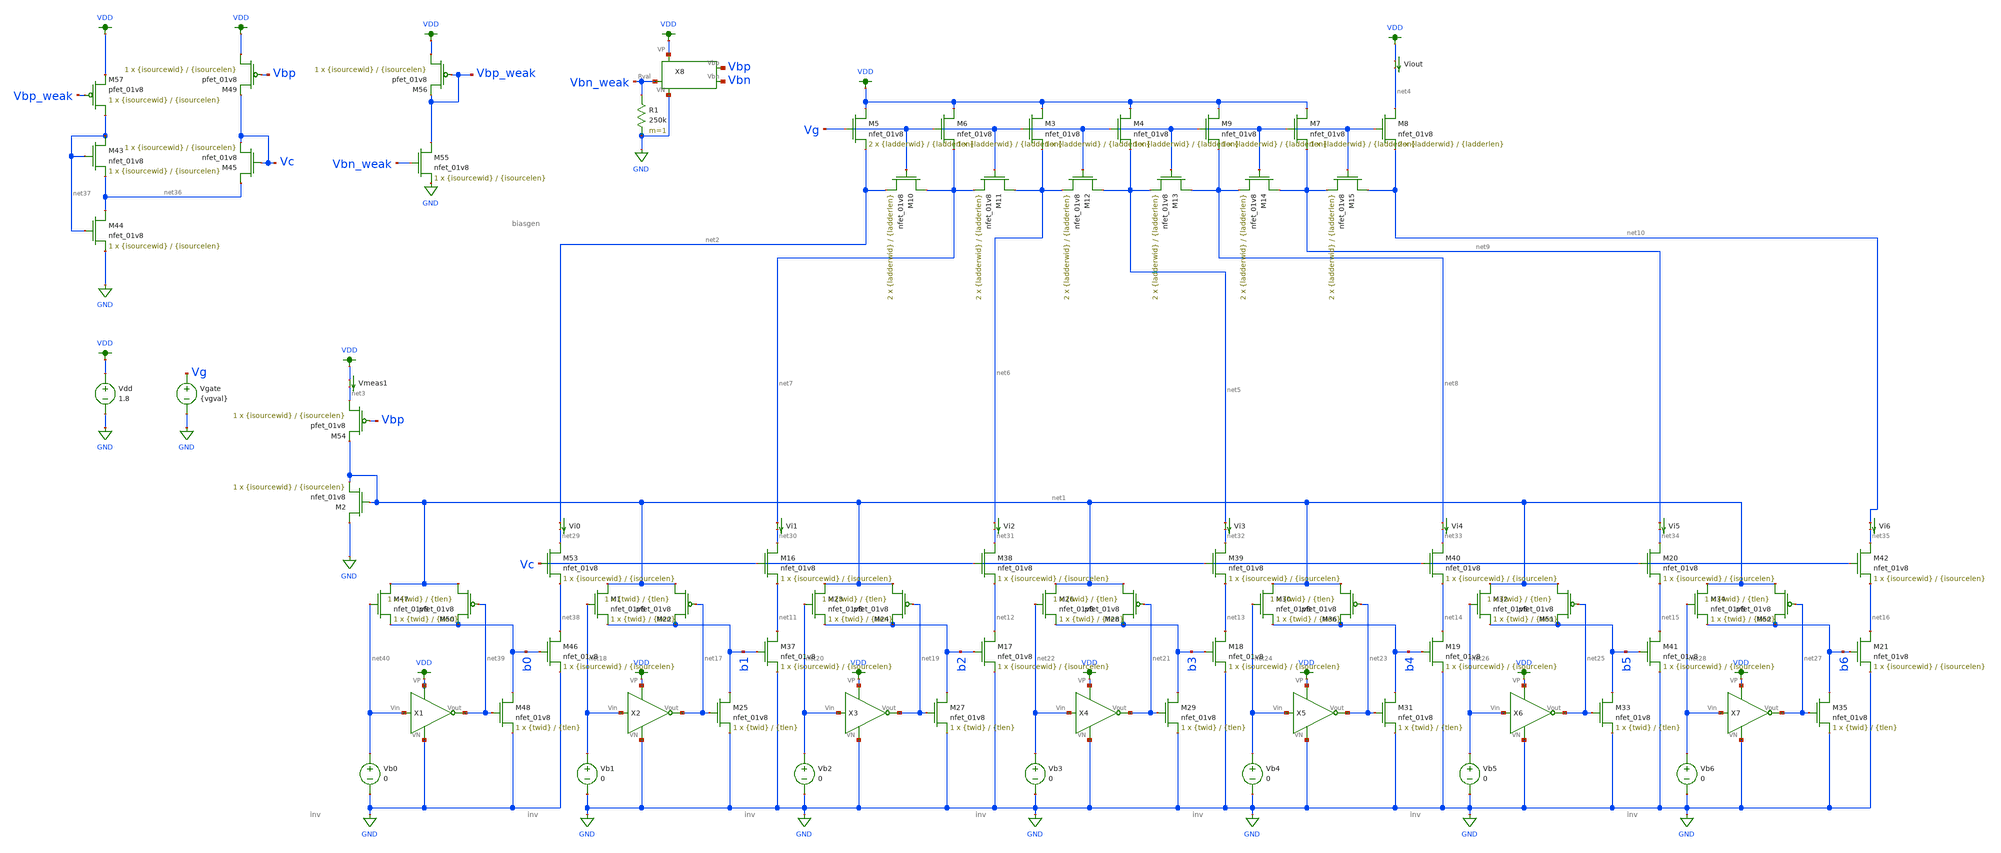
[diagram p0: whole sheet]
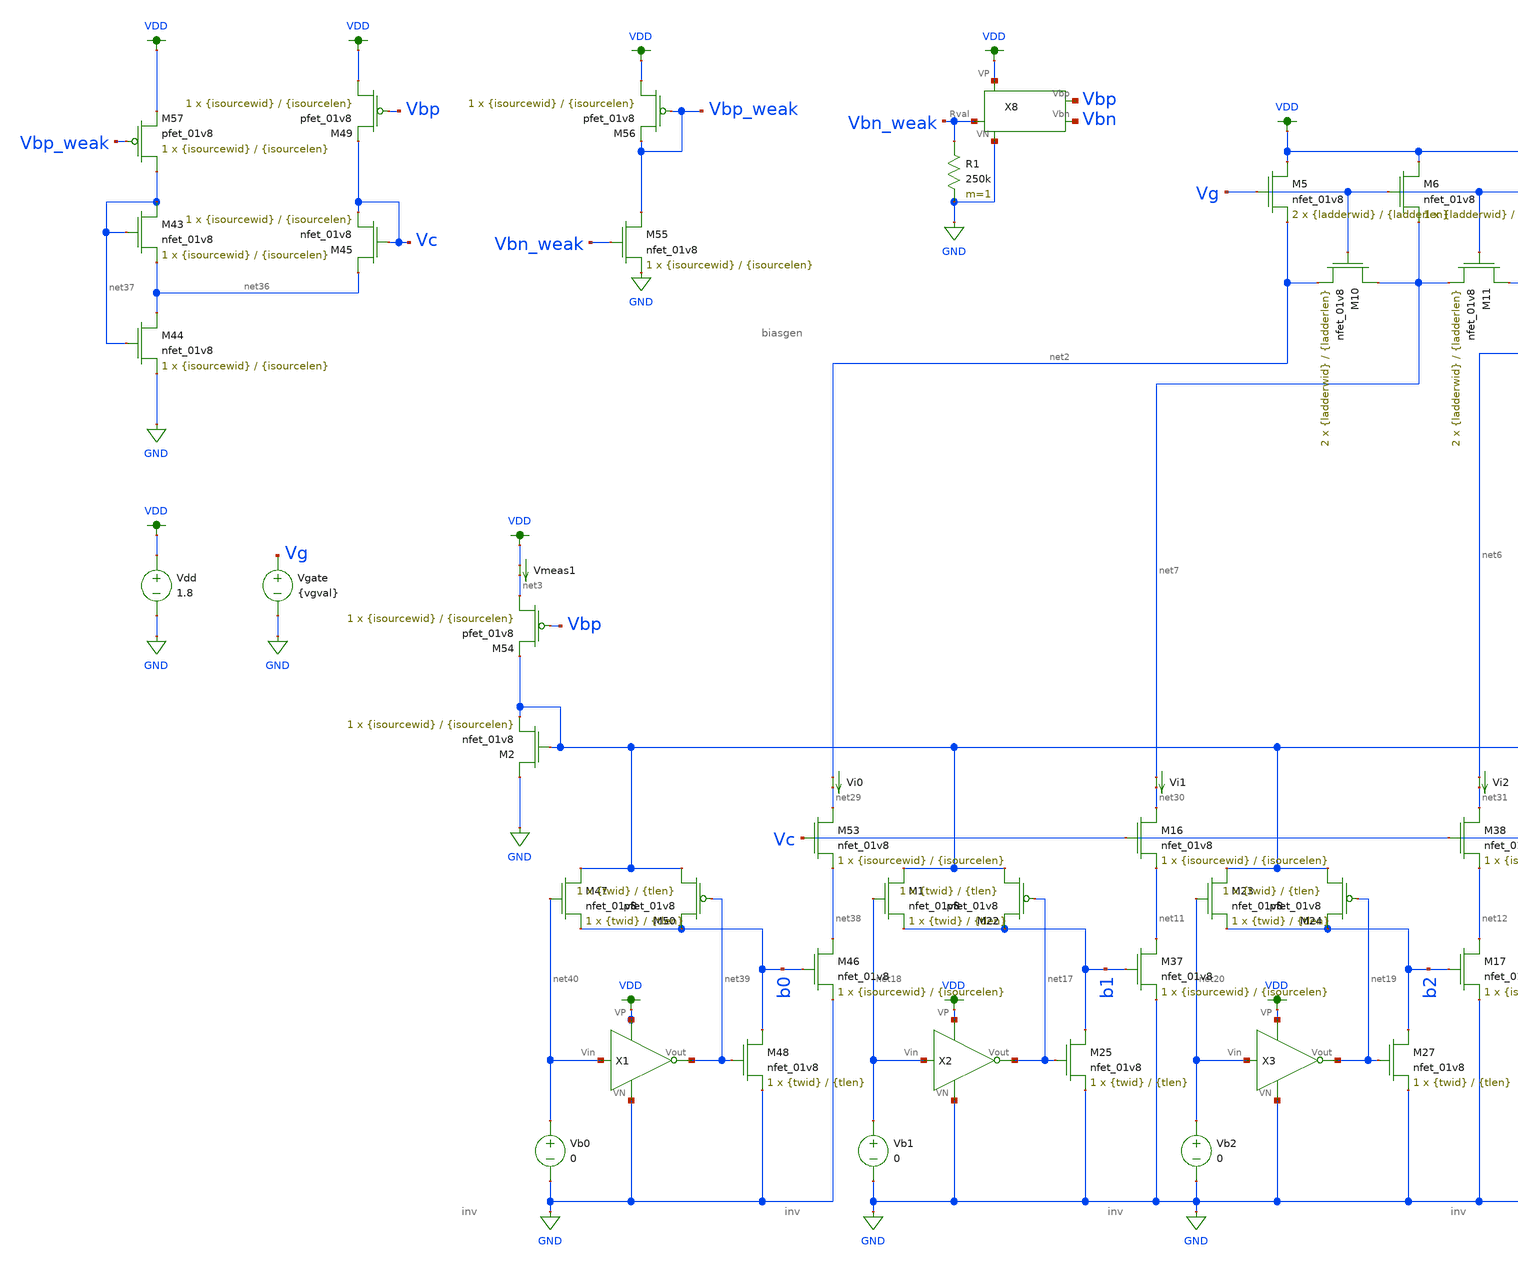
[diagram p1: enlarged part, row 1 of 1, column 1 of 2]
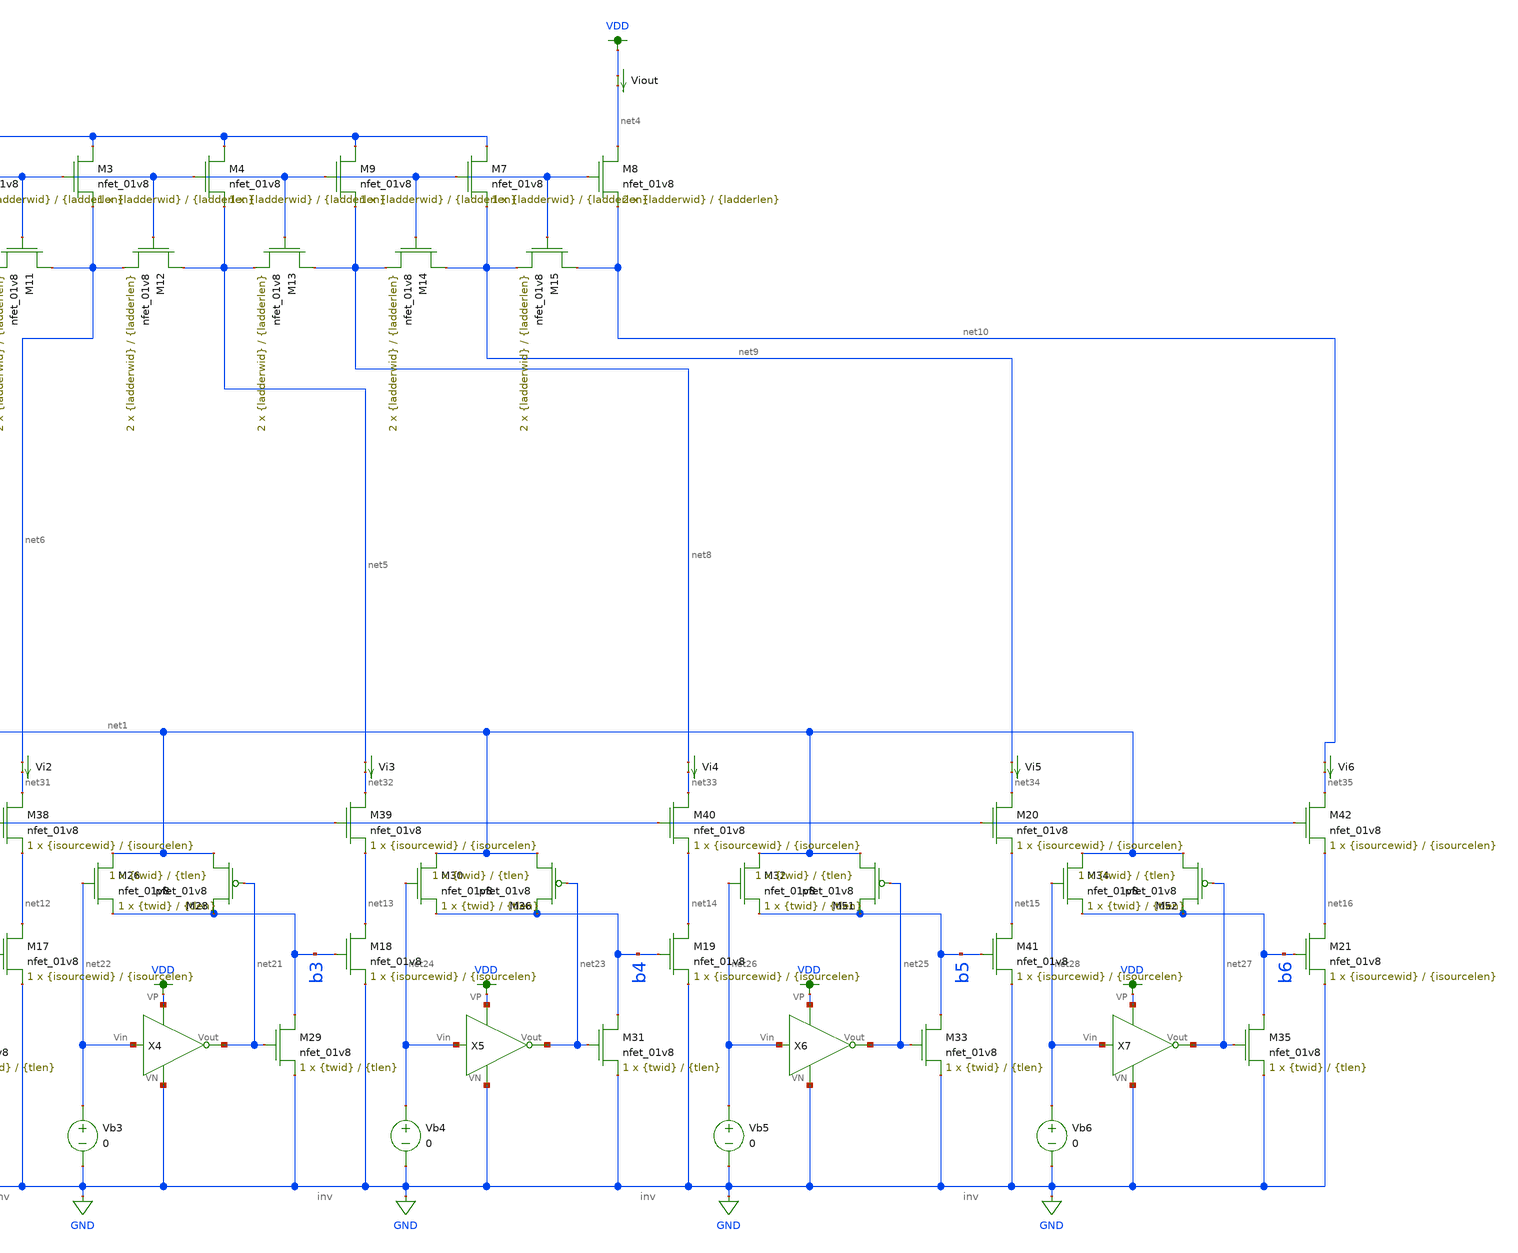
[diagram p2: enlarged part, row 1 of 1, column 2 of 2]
** sch_path: prelim-files/testing.sch
**.subckt testing
XM2 GND net1 net1 GND sky130_fd_pr__nfet_01v8 L={isourcelen} W={isourcewid} nf=1 ad='int((nf+1)/2) * W/nf * 0.29'
+ as='int((nf+2)/2) * W/nf * 0.29' pd='2*int((nf+1)/2) * (W/nf + 0.29)' ps='2*int((nf+2)/2) * (W/nf + 0.29)'
+ nrd='0.29 / W' nrs='0.29 / W' sa=0 sb=0 sd=0 mult=1 m=1
Vdd VDD GND 1.8
Vi0 net2 net29 0
.save i(vi0)
Vmeas1 VDD net3 0
.save i(vmeas1)
XM5 VDD Vg net2 GND sky130_fd_pr__nfet_01v8 L={ladderlen} W={ladderwid} nf=1 ad='int((nf+1)/2) * W/nf * 0.29'
+ as='int((nf+2)/2) * W/nf * 0.29' pd='2*int((nf+1)/2) * (W/nf + 0.29)' ps='2*int((nf+2)/2) * (W/nf + 0.29)'
+ nrd='0.29 / W' nrs='0.29 / W' sa=0 sb=0 sd=0 mult=2 m=2
XM6 VDD Vg net7 GND sky130_fd_pr__nfet_01v8 L={ladderlen} W={ladderwid} nf=1 ad='int((nf+1)/2) * W/nf * 0.29'
+ as='int((nf+2)/2) * W/nf * 0.29' pd='2*int((nf+1)/2) * (W/nf + 0.29)' ps='2*int((nf+2)/2) * (W/nf + 0.29)'
+ nrd='0.29 / W' nrs='0.29 / W' sa=0 sb=0 sd=0 mult=1 m=1
Viout VDD net4 0
.save i(viout)
Vb1 net18 GND 0
Vb2 net20 GND 0
Vgate Vg GND {vgval}
Vi1 net7 net30 0
.save i(vi1)
Vi2 net6 net31 0
.save i(vi2)
Vb3 net22 GND 0
Vi3 net5 net32 0
.save i(vi3)
Vb4 net24 GND 0
Vi4 net8 net33 0
.save i(vi4)
Vb5 net26 GND 0
Vi5 net9 net34 0
.save i(vi5)
Vb6 net28 GND 0
Vi6 net10 net35 0
.save i(vi6)
X2 net18 net17 VDD GND inv
XM25 b1 net17 GND GND sky130_fd_pr__nfet_01v8 L={tlen} W={twid} nf=1 ad='int((nf+1)/2) * W/nf * 0.29'
+ as='int((nf+2)/2) * W/nf * 0.29' pd='2*int((nf+1)/2) * (W/nf + 0.29)' ps='2*int((nf+2)/2) * (W/nf + 0.29)'
+ nrd='0.29 / W' nrs='0.29 / W' sa=0 sb=0 sd=0 mult=1 m=1
X3 net20 net19 VDD GND inv
XM27 b2 net19 GND GND sky130_fd_pr__nfet_01v8 L={tlen} W={twid} nf=1 ad='int((nf+1)/2) * W/nf * 0.29'
+ as='int((nf+2)/2) * W/nf * 0.29' pd='2*int((nf+1)/2) * (W/nf + 0.29)' ps='2*int((nf+2)/2) * (W/nf + 0.29)'
+ nrd='0.29 / W' nrs='0.29 / W' sa=0 sb=0 sd=0 mult=1 m=1
X4 net22 net21 VDD GND inv
XM29 b3 net21 GND GND sky130_fd_pr__nfet_01v8 L={tlen} W={twid} nf=1 ad='int((nf+1)/2) * W/nf * 0.29'
+ as='int((nf+2)/2) * W/nf * 0.29' pd='2*int((nf+1)/2) * (W/nf + 0.29)' ps='2*int((nf+2)/2) * (W/nf + 0.29)'
+ nrd='0.29 / W' nrs='0.29 / W' sa=0 sb=0 sd=0 mult=1 m=1
X5 net24 net23 VDD GND inv
XM31 b4 net23 GND GND sky130_fd_pr__nfet_01v8 L={tlen} W={twid} nf=1 ad='int((nf+1)/2) * W/nf * 0.29'
+ as='int((nf+2)/2) * W/nf * 0.29' pd='2*int((nf+1)/2) * (W/nf + 0.29)' ps='2*int((nf+2)/2) * (W/nf + 0.29)'
+ nrd='0.29 / W' nrs='0.29 / W' sa=0 sb=0 sd=0 mult=1 m=1
X6 net26 net25 VDD GND inv
XM33 b5 net25 GND GND sky130_fd_pr__nfet_01v8 L={tlen} W={twid} nf=1 ad='int((nf+1)/2) * W/nf * 0.29'
+ as='int((nf+2)/2) * W/nf * 0.29' pd='2*int((nf+1)/2) * (W/nf + 0.29)' ps='2*int((nf+2)/2) * (W/nf + 0.29)'
+ nrd='0.29 / W' nrs='0.29 / W' sa=0 sb=0 sd=0 mult=1 m=1
X7 net28 net27 VDD GND inv
XM35 b6 net27 GND GND sky130_fd_pr__nfet_01v8 L={tlen} W={twid} nf=1 ad='int((nf+1)/2) * W/nf * 0.29'
+ as='int((nf+2)/2) * W/nf * 0.29' pd='2*int((nf+1)/2) * (W/nf + 0.29)' ps='2*int((nf+2)/2) * (W/nf + 0.29)'
+ nrd='0.29 / W' nrs='0.29 / W' sa=0 sb=0 sd=0 mult=1 m=1
XM43 net37 net37 net36 GND sky130_fd_pr__nfet_01v8 L={isourcelen} W={isourcewid} nf=1 ad='int((nf+1)/2) * W/nf * 0.29'
+ as='int((nf+2)/2) * W/nf * 0.29' pd='2*int((nf+1)/2) * (W/nf + 0.29)' ps='2*int((nf+2)/2) * (W/nf + 0.29)'
+ nrd='0.29 / W' nrs='0.29 / W' sa=0 sb=0 sd=0 mult=1 m=1
XM44 net36 net37 GND GND sky130_fd_pr__nfet_01v8 L={isourcelen} W={isourcewid} nf=1 ad='int((nf+1)/2) * W/nf * 0.29'
+ as='int((nf+2)/2) * W/nf * 0.29' pd='2*int((nf+1)/2) * (W/nf + 0.29)' ps='2*int((nf+2)/2) * (W/nf + 0.29)'
+ nrd='0.29 / W' nrs='0.29 / W' sa=0 sb=0 sd=0 mult=1 m=1
XM45 net36 Vc Vc GND sky130_fd_pr__nfet_01v8 L={isourcelen} W={isourcewid} nf=1 ad='int((nf+1)/2) * W/nf * 0.29'
+ as='int((nf+2)/2) * W/nf * 0.29' pd='2*int((nf+1)/2) * (W/nf + 0.29)' ps='2*int((nf+2)/2) * (W/nf + 0.29)'
+ nrd='0.29 / W' nrs='0.29 / W' sa=0 sb=0 sd=0 mult=1 m=1
Vb0 net40 GND 0
X1 net40 net39 VDD GND inv
XM47 net1 net40 b0 GND sky130_fd_pr__nfet_01v8 L={tlen} W={twid} nf=1 ad='int((nf+1)/2) * W/nf * 0.29'
+ as='int((nf+2)/2) * W/nf * 0.29' pd='2*int((nf+1)/2) * (W/nf + 0.29)' ps='2*int((nf+2)/2) * (W/nf + 0.29)'
+ nrd='0.29 / W' nrs='0.29 / W' sa=0 sb=0 sd=0 mult=1 m=1
XM48 b0 net39 GND GND sky130_fd_pr__nfet_01v8 L={tlen} W={twid} nf=1 ad='int((nf+1)/2) * W/nf * 0.29'
+ as='int((nf+2)/2) * W/nf * 0.29' pd='2*int((nf+1)/2) * (W/nf + 0.29)' ps='2*int((nf+2)/2) * (W/nf + 0.29)'
+ nrd='0.29 / W' nrs='0.29 / W' sa=0 sb=0 sd=0 mult=1 m=1
XM50 net1 net39 b0 VDD sky130_fd_pr__pfet_01v8 L={tlen} W={twid} nf=1 ad='int((nf+1)/2) * W/nf * 0.29'
+ as='int((nf+2)/2) * W/nf * 0.29' pd='2*int((nf+1)/2) * (W/nf + 0.29)' ps='2*int((nf+2)/2) * (W/nf + 0.29)'
+ nrd='0.29 / W' nrs='0.29 / W' sa=0 sb=0 sd=0 mult=1 m=1
XM1 net1 net18 b1 GND sky130_fd_pr__nfet_01v8 L={tlen} W={twid} nf=1 ad='int((nf+1)/2) * W/nf * 0.29'
+ as='int((nf+2)/2) * W/nf * 0.29' pd='2*int((nf+1)/2) * (W/nf + 0.29)' ps='2*int((nf+2)/2) * (W/nf + 0.29)'
+ nrd='0.29 / W' nrs='0.29 / W' sa=0 sb=0 sd=0 mult=1 m=1
XM22 net1 net17 b1 VDD sky130_fd_pr__pfet_01v8 L={tlen} W={twid} nf=1 ad='int((nf+1)/2) * W/nf * 0.29'
+ as='int((nf+2)/2) * W/nf * 0.29' pd='2*int((nf+1)/2) * (W/nf + 0.29)' ps='2*int((nf+2)/2) * (W/nf + 0.29)'
+ nrd='0.29 / W' nrs='0.29 / W' sa=0 sb=0 sd=0 mult=1 m=1
XM23 net1 net20 b2 GND sky130_fd_pr__nfet_01v8 L={tlen} W={twid} nf=1 ad='int((nf+1)/2) * W/nf * 0.29'
+ as='int((nf+2)/2) * W/nf * 0.29' pd='2*int((nf+1)/2) * (W/nf + 0.29)' ps='2*int((nf+2)/2) * (W/nf + 0.29)'
+ nrd='0.29 / W' nrs='0.29 / W' sa=0 sb=0 sd=0 mult=1 m=1
XM24 net1 net19 b2 VDD sky130_fd_pr__pfet_01v8 L={tlen} W={twid} nf=1 ad='int((nf+1)/2) * W/nf * 0.29'
+ as='int((nf+2)/2) * W/nf * 0.29' pd='2*int((nf+1)/2) * (W/nf + 0.29)' ps='2*int((nf+2)/2) * (W/nf + 0.29)'
+ nrd='0.29 / W' nrs='0.29 / W' sa=0 sb=0 sd=0 mult=1 m=1
XM26 net1 net22 b3 GND sky130_fd_pr__nfet_01v8 L={tlen} W={twid} nf=1 ad='int((nf+1)/2) * W/nf * 0.29'
+ as='int((nf+2)/2) * W/nf * 0.29' pd='2*int((nf+1)/2) * (W/nf + 0.29)' ps='2*int((nf+2)/2) * (W/nf + 0.29)'
+ nrd='0.29 / W' nrs='0.29 / W' sa=0 sb=0 sd=0 mult=1 m=1
XM28 net1 net21 b3 VDD sky130_fd_pr__pfet_01v8 L={tlen} W={twid} nf=1 ad='int((nf+1)/2) * W/nf * 0.29'
+ as='int((nf+2)/2) * W/nf * 0.29' pd='2*int((nf+1)/2) * (W/nf + 0.29)' ps='2*int((nf+2)/2) * (W/nf + 0.29)'
+ nrd='0.29 / W' nrs='0.29 / W' sa=0 sb=0 sd=0 mult=1 m=1
XM30 net1 net24 b4 GND sky130_fd_pr__nfet_01v8 L={tlen} W={twid} nf=1 ad='int((nf+1)/2) * W/nf * 0.29'
+ as='int((nf+2)/2) * W/nf * 0.29' pd='2*int((nf+1)/2) * (W/nf + 0.29)' ps='2*int((nf+2)/2) * (W/nf + 0.29)'
+ nrd='0.29 / W' nrs='0.29 / W' sa=0 sb=0 sd=0 mult=1 m=1
XM36 net1 net23 b4 VDD sky130_fd_pr__pfet_01v8 L={tlen} W={twid} nf=1 ad='int((nf+1)/2) * W/nf * 0.29'
+ as='int((nf+2)/2) * W/nf * 0.29' pd='2*int((nf+1)/2) * (W/nf + 0.29)' ps='2*int((nf+2)/2) * (W/nf + 0.29)'
+ nrd='0.29 / W' nrs='0.29 / W' sa=0 sb=0 sd=0 mult=1 m=1
XM32 net1 net26 b5 GND sky130_fd_pr__nfet_01v8 L={tlen} W={twid} nf=1 ad='int((nf+1)/2) * W/nf * 0.29'
+ as='int((nf+2)/2) * W/nf * 0.29' pd='2*int((nf+1)/2) * (W/nf + 0.29)' ps='2*int((nf+2)/2) * (W/nf + 0.29)'
+ nrd='0.29 / W' nrs='0.29 / W' sa=0 sb=0 sd=0 mult=1 m=1
XM51 net1 net25 b5 VDD sky130_fd_pr__pfet_01v8 L={tlen} W={twid} nf=1 ad='int((nf+1)/2) * W/nf * 0.29'
+ as='int((nf+2)/2) * W/nf * 0.29' pd='2*int((nf+1)/2) * (W/nf + 0.29)' ps='2*int((nf+2)/2) * (W/nf + 0.29)'
+ nrd='0.29 / W' nrs='0.29 / W' sa=0 sb=0 sd=0 mult=1 m=1
XM34 net1 net28 b6 GND sky130_fd_pr__nfet_01v8 L={tlen} W={twid} nf=1 ad='int((nf+1)/2) * W/nf * 0.29'
+ as='int((nf+2)/2) * W/nf * 0.29' pd='2*int((nf+1)/2) * (W/nf + 0.29)' ps='2*int((nf+2)/2) * (W/nf + 0.29)'
+ nrd='0.29 / W' nrs='0.29 / W' sa=0 sb=0 sd=0 mult=1 m=1
XM52 net1 net27 b6 VDD sky130_fd_pr__pfet_01v8 L={tlen} W={twid} nf=1 ad='int((nf+1)/2) * W/nf * 0.29'
+ as='int((nf+2)/2) * W/nf * 0.29' pd='2*int((nf+1)/2) * (W/nf + 0.29)' ps='2*int((nf+2)/2) * (W/nf + 0.29)'
+ nrd='0.29 / W' nrs='0.29 / W' sa=0 sb=0 sd=0 mult=1 m=1
XM10 net7 Vg net2 GND sky130_fd_pr__nfet_01v8 L={ladderlen} W={ladderwid} nf=1 ad='int((nf+1)/2) * W/nf * 0.29'
+ as='int((nf+2)/2) * W/nf * 0.29' pd='2*int((nf+1)/2) * (W/nf + 0.29)' ps='2*int((nf+2)/2) * (W/nf + 0.29)'
+ nrd='0.29 / W' nrs='0.29 / W' sa=0 sb=0 sd=0 mult=2 m=2
XM11 net6 Vg net7 GND sky130_fd_pr__nfet_01v8 L={ladderlen} W={ladderwid} nf=1 ad='int((nf+1)/2) * W/nf * 0.29'
+ as='int((nf+2)/2) * W/nf * 0.29' pd='2*int((nf+1)/2) * (W/nf + 0.29)' ps='2*int((nf+2)/2) * (W/nf + 0.29)'
+ nrd='0.29 / W' nrs='0.29 / W' sa=0 sb=0 sd=0 mult=2 m=2
XM12 net5 Vg net6 GND sky130_fd_pr__nfet_01v8 L={ladderlen} W={ladderwid} nf=1 ad='int((nf+1)/2) * W/nf * 0.29'
+ as='int((nf+2)/2) * W/nf * 0.29' pd='2*int((nf+1)/2) * (W/nf + 0.29)' ps='2*int((nf+2)/2) * (W/nf + 0.29)'
+ nrd='0.29 / W' nrs='0.29 / W' sa=0 sb=0 sd=0 mult=2 m=2
XM13 net8 Vg net5 GND sky130_fd_pr__nfet_01v8 L={ladderlen} W={ladderwid} nf=1 ad='int((nf+1)/2) * W/nf * 0.29'
+ as='int((nf+2)/2) * W/nf * 0.29' pd='2*int((nf+1)/2) * (W/nf + 0.29)' ps='2*int((nf+2)/2) * (W/nf + 0.29)'
+ nrd='0.29 / W' nrs='0.29 / W' sa=0 sb=0 sd=0 mult=2 m=2
XM14 net9 Vg net8 GND sky130_fd_pr__nfet_01v8 L={ladderlen} W={ladderwid} nf=1 ad='int((nf+1)/2) * W/nf * 0.29'
+ as='int((nf+2)/2) * W/nf * 0.29' pd='2*int((nf+1)/2) * (W/nf + 0.29)' ps='2*int((nf+2)/2) * (W/nf + 0.29)'
+ nrd='0.29 / W' nrs='0.29 / W' sa=0 sb=0 sd=0 mult=2 m=2
XM15 net10 Vg net9 GND sky130_fd_pr__nfet_01v8 L={ladderlen} W={ladderwid} nf=1 ad='int((nf+1)/2) * W/nf * 0.29'
+ as='int((nf+2)/2) * W/nf * 0.29' pd='2*int((nf+1)/2) * (W/nf + 0.29)' ps='2*int((nf+2)/2) * (W/nf + 0.29)'
+ nrd='0.29 / W' nrs='0.29 / W' sa=0 sb=0 sd=0 mult=2 m=2
XM8 net4 Vg net10 GND sky130_fd_pr__nfet_01v8 L={ladderlen} W={ladderwid} nf=1 ad='int((nf+1)/2) * W/nf * 0.29'
+ as='int((nf+2)/2) * W/nf * 0.29' pd='2*int((nf+1)/2) * (W/nf + 0.29)' ps='2*int((nf+2)/2) * (W/nf + 0.29)'
+ nrd='0.29 / W' nrs='0.29 / W' sa=0 sb=0 sd=0 mult=2 m=2
XM3 VDD Vg net6 GND sky130_fd_pr__nfet_01v8 L={ladderlen} W={ladderwid} nf=1 ad='int((nf+1)/2) * W/nf * 0.29'
+ as='int((nf+2)/2) * W/nf * 0.29' pd='2*int((nf+1)/2) * (W/nf + 0.29)' ps='2*int((nf+2)/2) * (W/nf + 0.29)'
+ nrd='0.29 / W' nrs='0.29 / W' sa=0 sb=0 sd=0 mult=1 m=1
XM4 VDD Vg net5 GND sky130_fd_pr__nfet_01v8 L={ladderlen} W={ladderwid} nf=1 ad='int((nf+1)/2) * W/nf * 0.29'
+ as='int((nf+2)/2) * W/nf * 0.29' pd='2*int((nf+1)/2) * (W/nf + 0.29)' ps='2*int((nf+2)/2) * (W/nf + 0.29)'
+ nrd='0.29 / W' nrs='0.29 / W' sa=0 sb=0 sd=0 mult=1 m=1
XM9 VDD Vg net8 GND sky130_fd_pr__nfet_01v8 L={ladderlen} W={ladderwid} nf=1 ad='int((nf+1)/2) * W/nf * 0.29'
+ as='int((nf+2)/2) * W/nf * 0.29' pd='2*int((nf+1)/2) * (W/nf + 0.29)' ps='2*int((nf+2)/2) * (W/nf + 0.29)'
+ nrd='0.29 / W' nrs='0.29 / W' sa=0 sb=0 sd=0 mult=1 m=1
XM7 VDD Vg net9 GND sky130_fd_pr__nfet_01v8 L={ladderlen} W={ladderwid} nf=1 ad='int((nf+1)/2) * W/nf * 0.29'
+ as='int((nf+2)/2) * W/nf * 0.29' pd='2*int((nf+1)/2) * (W/nf + 0.29)' ps='2*int((nf+2)/2) * (W/nf + 0.29)'
+ nrd='0.29 / W' nrs='0.29 / W' sa=0 sb=0 sd=0 mult=1 m=1
XM53 net29 Vc net38 GND sky130_fd_pr__nfet_01v8 L={isourcelen} W={isourcewid} nf=1 ad='int((nf+1)/2) * W/nf * 0.29'
+ as='int((nf+2)/2) * W/nf * 0.29' pd='2*int((nf+1)/2) * (W/nf + 0.29)' ps='2*int((nf+2)/2) * (W/nf + 0.29)'
+ nrd='0.29 / W' nrs='0.29 / W' sa=0 sb=0 sd=0 mult=1 m=1
XM46 net38 b0 GND GND sky130_fd_pr__nfet_01v8 L={isourcelen} W={isourcewid} nf=1 ad='int((nf+1)/2) * W/nf * 0.29'
+ as='int((nf+2)/2) * W/nf * 0.29' pd='2*int((nf+1)/2) * (W/nf + 0.29)' ps='2*int((nf+2)/2) * (W/nf + 0.29)'
+ nrd='0.29 / W' nrs='0.29 / W' sa=0 sb=0 sd=0 mult=1 m=1
XM37 net11 b1 GND GND sky130_fd_pr__nfet_01v8 L={isourcelen} W={isourcewid} nf=1 ad='int((nf+1)/2) * W/nf * 0.29'
+ as='int((nf+2)/2) * W/nf * 0.29' pd='2*int((nf+1)/2) * (W/nf + 0.29)' ps='2*int((nf+2)/2) * (W/nf + 0.29)'
+ nrd='0.29 / W' nrs='0.29 / W' sa=0 sb=0 sd=0 mult=1 m=1
XM16 net30 Vc net11 GND sky130_fd_pr__nfet_01v8 L={isourcelen} W={isourcewid} nf=1 ad='int((nf+1)/2) * W/nf * 0.29'
+ as='int((nf+2)/2) * W/nf * 0.29' pd='2*int((nf+1)/2) * (W/nf + 0.29)' ps='2*int((nf+2)/2) * (W/nf + 0.29)'
+ nrd='0.29 / W' nrs='0.29 / W' sa=0 sb=0 sd=0 mult=1 m=1
XM17 net12 b2 GND GND sky130_fd_pr__nfet_01v8 L={isourcelen} W={isourcewid} nf=1 ad='int((nf+1)/2) * W/nf * 0.29'
+ as='int((nf+2)/2) * W/nf * 0.29' pd='2*int((nf+1)/2) * (W/nf + 0.29)' ps='2*int((nf+2)/2) * (W/nf + 0.29)'
+ nrd='0.29 / W' nrs='0.29 / W' sa=0 sb=0 sd=0 mult=1 m=1
XM38 net31 Vc net12 GND sky130_fd_pr__nfet_01v8 L={isourcelen} W={isourcewid} nf=1 ad='int((nf+1)/2) * W/nf * 0.29'
+ as='int((nf+2)/2) * W/nf * 0.29' pd='2*int((nf+1)/2) * (W/nf + 0.29)' ps='2*int((nf+2)/2) * (W/nf + 0.29)'
+ nrd='0.29 / W' nrs='0.29 / W' sa=0 sb=0 sd=0 mult=1 m=1
XM18 net13 b3 GND GND sky130_fd_pr__nfet_01v8 L={isourcelen} W={isourcewid} nf=1 ad='int((nf+1)/2) * W/nf * 0.29'
+ as='int((nf+2)/2) * W/nf * 0.29' pd='2*int((nf+1)/2) * (W/nf + 0.29)' ps='2*int((nf+2)/2) * (W/nf + 0.29)'
+ nrd='0.29 / W' nrs='0.29 / W' sa=0 sb=0 sd=0 mult=1 m=1
XM39 net32 Vc net13 GND sky130_fd_pr__nfet_01v8 L={isourcelen} W={isourcewid} nf=1 ad='int((nf+1)/2) * W/nf * 0.29'
+ as='int((nf+2)/2) * W/nf * 0.29' pd='2*int((nf+1)/2) * (W/nf + 0.29)' ps='2*int((nf+2)/2) * (W/nf + 0.29)'
+ nrd='0.29 / W' nrs='0.29 / W' sa=0 sb=0 sd=0 mult=1 m=1
XM19 net14 b4 GND GND sky130_fd_pr__nfet_01v8 L={isourcelen} W={isourcewid} nf=1 ad='int((nf+1)/2) * W/nf * 0.29'
+ as='int((nf+2)/2) * W/nf * 0.29' pd='2*int((nf+1)/2) * (W/nf + 0.29)' ps='2*int((nf+2)/2) * (W/nf + 0.29)'
+ nrd='0.29 / W' nrs='0.29 / W' sa=0 sb=0 sd=0 mult=1 m=1
XM40 net33 Vc net14 GND sky130_fd_pr__nfet_01v8 L={isourcelen} W={isourcewid} nf=1 ad='int((nf+1)/2) * W/nf * 0.29'
+ as='int((nf+2)/2) * W/nf * 0.29' pd='2*int((nf+1)/2) * (W/nf + 0.29)' ps='2*int((nf+2)/2) * (W/nf + 0.29)'
+ nrd='0.29 / W' nrs='0.29 / W' sa=0 sb=0 sd=0 mult=1 m=1
XM20 net34 Vc net15 GND sky130_fd_pr__nfet_01v8 L={isourcelen} W={isourcewid} nf=1 ad='int((nf+1)/2) * W/nf * 0.29'
+ as='int((nf+2)/2) * W/nf * 0.29' pd='2*int((nf+1)/2) * (W/nf + 0.29)' ps='2*int((nf+2)/2) * (W/nf + 0.29)'
+ nrd='0.29 / W' nrs='0.29 / W' sa=0 sb=0 sd=0 mult=1 m=1
XM41 net15 b5 GND GND sky130_fd_pr__nfet_01v8 L={isourcelen} W={isourcewid} nf=1 ad='int((nf+1)/2) * W/nf * 0.29'
+ as='int((nf+2)/2) * W/nf * 0.29' pd='2*int((nf+1)/2) * (W/nf + 0.29)' ps='2*int((nf+2)/2) * (W/nf + 0.29)'
+ nrd='0.29 / W' nrs='0.29 / W' sa=0 sb=0 sd=0 mult=1 m=1
XM21 net16 b6 GND GND sky130_fd_pr__nfet_01v8 L={isourcelen} W={isourcewid} nf=1 ad='int((nf+1)/2) * W/nf * 0.29'
+ as='int((nf+2)/2) * W/nf * 0.29' pd='2*int((nf+1)/2) * (W/nf + 0.29)' ps='2*int((nf+2)/2) * (W/nf + 0.29)'
+ nrd='0.29 / W' nrs='0.29 / W' sa=0 sb=0 sd=0 mult=1 m=1
XM42 net35 Vc net16 GND sky130_fd_pr__nfet_01v8 L={isourcelen} W={isourcewid} nf=1 ad='int((nf+1)/2) * W/nf * 0.29'
+ as='int((nf+2)/2) * W/nf * 0.29' pd='2*int((nf+1)/2) * (W/nf + 0.29)' ps='2*int((nf+2)/2) * (W/nf + 0.29)'
+ nrd='0.29 / W' nrs='0.29 / W' sa=0 sb=0 sd=0 mult=1 m=1
X8 Vbn_weak GND VDD Vbp Vbn biasgen
R1 Vbn_weak GND 250k m=1
XM49 VDD Vbp Vc VDD sky130_fd_pr__pfet_01v8 L={isourcelen} W={isourcewid} nf=1 ad='int((nf+1)/2) * W/nf * 0.29'
+ as='int((nf+2)/2) * W/nf * 0.29' pd='2*int((nf+1)/2) * (W/nf + 0.29)' ps='2*int((nf+2)/2) * (W/nf + 0.29)'
+ nrd='0.29 / W' nrs='0.29 / W' sa=0 sb=0 sd=0 mult=1 m=1
XM54 net3 Vbp net1 VDD sky130_fd_pr__pfet_01v8 L={isourcelen} W={isourcewid} nf=1 ad='int((nf+1)/2) * W/nf * 0.29'
+ as='int((nf+2)/2) * W/nf * 0.29' pd='2*int((nf+1)/2) * (W/nf + 0.29)' ps='2*int((nf+2)/2) * (W/nf + 0.29)'
+ nrd='0.29 / W' nrs='0.29 / W' sa=0 sb=0 sd=0 mult=1 m=1
XM55 Vbp_weak Vbn_weak GND GND sky130_fd_pr__nfet_01v8 L={isourcelen} W={isourcewid} nf=1 ad='int((nf+1)/2) * W/nf * 0.29'
+ as='int((nf+2)/2) * W/nf * 0.29' pd='2*int((nf+1)/2) * (W/nf + 0.29)' ps='2*int((nf+2)/2) * (W/nf + 0.29)'
+ nrd='0.29 / W' nrs='0.29 / W' sa=0 sb=0 sd=0 mult=1 m=1
XM56 VDD Vbp_weak Vbp_weak VDD sky130_fd_pr__pfet_01v8 L={isourcelen} W={isourcewid} nf=1 ad='int((nf+1)/2) * W/nf * 0.29'
+ as='int((nf+2)/2) * W/nf * 0.29' pd='2*int((nf+1)/2) * (W/nf + 0.29)' ps='2*int((nf+2)/2) * (W/nf + 0.29)'
+ nrd='0.29 / W' nrs='0.29 / W' sa=0 sb=0 sd=0 mult=1 m=1
XM57 net37 Vbp_weak VDD VDD sky130_fd_pr__pfet_01v8 L={isourcelen} W={isourcewid} nf=1 ad='int((nf+1)/2) * W/nf * 0.29'
+ as='int((nf+2)/2) * W/nf * 0.29' pd='2*int((nf+1)/2) * (W/nf + 0.29)' ps='2*int((nf+2)/2) * (W/nf + 0.29)'
+ nrd='0.29 / W' nrs='0.29 / W' sa=0 sb=0 sd=0 mult=1 m=1
**** begin user architecture code

.option wnflag=1
.param MC_SWITCH=0.0
.lib ~/skywater/skywater-pdk/libraries/sky130_fd_pr_ngspice/latest/models/sky130.lib.spice tt


.param M=8
.param vgval=1.8
.param tlen=0.3
.param twid=3.15
.param ladderlen=1.4
.param ladderwid=5.7
.param isourcelen=0.5
.param isourcewid=1.4
.control
	set wr_vecnames
	set wr_singlescale
	let code = 0
	while code < 128
		if code eq 0
			let nb0 = 0
		else
			let nb0 = (code % 2)*1.8
		end
		if floor(code / 2) eq 0
			let nb1 = 0
		else
			let nb1 = (floor(code / 2) % 2)*1.8
		end
		if floor(code / 4) eq 0
			let nb2 = 0
		else
			let nb2 = (floor(code / 4) % 2)*1.8
		end
		if floor(code / 8) eq 0
			let nb3 = 0
		else
			let nb3 = (floor(code / 8) % 2)*1.8
		end
		if floor(code / 16) eq 0
			let nb4 = 0
		else
			let nb4 = (floor(code / 16) % 2)*1.8
		end
		if floor(code / 32) eq 0
			let nb5 = 0
		else
			let nb5 = (floor(code / 32) % 2)*1.8
		end
		if floor(code / 64) eq 0
			let nb6 = 0
		else
			let nb6 = (floor(code / 64) % 2)*1.8
		end
		alter Vb0 $&nb0
		alter Vb1 $&nb1
		alter Vb2 $&nb2
		alter Vb3 $&nb3
		alter Vb4 $&nb4
		alter Vb5 $&nb5
		alter Vb6 $&nb6
		save all
		op
		wrdata ~/VLSI/MP4/dacdata.txt i(Viout)
		if code eq 0
			set appendwrite
			set wr_vecnames = FALSE
		end
		let code = code + 1
	end
	quit
.endc

**** end user architecture code
**.ends

* expanding   symbol:  /home/jonah/VLSI/MP4/inv.sym # of pins=4
** sym_path: prelim-files/inv.sym
** sch_path: prelim-files/inv.sch
.subckt inv Vin Vout VP VN
*.iopin VP
*.iopin VN
*.ipin Vin
*.iopin Vout
XM1 Vout Vin VN GND sky130_fd_pr__nfet_01v8 L={tlen} W={twid} nf=1 ad='int((nf+1)/2) * W/nf * 0.29' as='int((nf+2)/2) * W/nf * 0.29'
+ pd='2*int((nf+1)/2) * (W/nf + 0.29)' ps='2*int((nf+2)/2) * (W/nf + 0.29)' nrd='0.29 / W' nrs='0.29 / W'
+ sa=0 sb=0 sd=0 mult=1 m=1
XM2 Vout Vin VP VDD sky130_fd_pr__pfet_01v8 L={tlen} W={twid} nf=1 ad='int((nf+1)/2) * W/nf * 0.29' as='int((nf+2)/2) * W/nf * 0.29'
+ pd='2*int((nf+1)/2) * (W/nf + 0.29)' ps='2*int((nf+2)/2) * (W/nf + 0.29)' nrd='0.29 / W' nrs='0.29 / W'
+ sa=0 sb=0 sd=0 mult=1 m=1
.ends


* expanding   symbol:  /home/jonah/VLSI/MP4/biasgen.sym # of pins=5
** sym_path: prelim-files/biasgen.sym
** sch_path: prelim-files/biasgen.sch
.subckt biasgen Rval VN VP Vbp Vbn
*.iopin Rval
*.iopin VN
*.iopin VP
*.iopin Vbp
*.iopin Vbn
XM1 net1 net2 VN GND sky130_fd_pr__nfet_01v8 L={isourcelen} W={isourcewid} nf=1 ad='int((nf+1)/2) * W/nf * 0.29'
+ as='int((nf+2)/2) * W/nf * 0.29' pd='2*int((nf+1)/2) * (W/nf + 0.29)' ps='2*int((nf+2)/2) * (W/nf + 0.29)'
+ nrd='0.29 / W' nrs='0.29 / W' sa=0 sb=0 sd=0 mult=1 m=1
XM5 Rval net2 net2 GND sky130_fd_pr__nfet_01v8 L={isourcelen} W={isourcewid} nf=1 ad='int((nf+1)/2) * W/nf * 0.29'
+ as='int((nf+2)/2) * W/nf * 0.29' pd='2*int((nf+1)/2) * (W/nf + 0.29)' ps='2*int((nf+2)/2) * (W/nf + 0.29)'
+ nrd='0.29 / W' nrs='0.29 / W' sa=0 sb=0 sd=0 mult={M} m={M}
Viout net3 Vbn 0
.save i(viout)
XM8 VP Vbp net2 VDD sky130_fd_pr__pfet_01v8 L={isourcelen} W={isourcewid} nf=1 ad='int((nf+1)/2) * W/nf * 0.29'
+ as='int((nf+2)/2) * W/nf * 0.29' pd='2*int((nf+1)/2) * (W/nf + 0.29)' ps='2*int((nf+2)/2) * (W/nf + 0.29)'
+ nrd='0.29 / W' nrs='0.29 / W' sa=0 sb=0 sd=0 mult=1 m=1
XM3 VP net1 net1 VDD sky130_fd_pr__pfet_01v8 L={isourcelen} W={isourcewid} nf=1 ad='int((nf+1)/2) * W/nf * 0.29'
+ as='int((nf+2)/2) * W/nf * 0.29' pd='2*int((nf+1)/2) * (W/nf + 0.29)' ps='2*int((nf+2)/2) * (W/nf + 0.29)'
+ nrd='0.29 / W' nrs='0.29 / W' sa=0 sb=0 sd=0 mult=1 m=1
XM2 Vbp net1 VP VDD sky130_fd_pr__pfet_01v8 L={isourcelen} W={isourcewid} nf=1 ad='int((nf+1)/2) * W/nf * 0.29'
+ as='int((nf+2)/2) * W/nf * 0.29' pd='2*int((nf+1)/2) * (W/nf + 0.29)' ps='2*int((nf+2)/2) * (W/nf + 0.29)'
+ nrd='0.29 / W' nrs='0.29 / W' sa=0 sb=0 sd=0 mult=1 m=1
XM7 net3 Vbp VP VDD sky130_fd_pr__pfet_01v8 L={isourcelen} W={isourcewid} nf=1 ad='int((nf+1)/2) * W/nf * 0.29'
+ as='int((nf+2)/2) * W/nf * 0.29' pd='2*int((nf+1)/2) * (W/nf + 0.29)' ps='2*int((nf+2)/2) * (W/nf + 0.29)'
+ nrd='0.29 / W' nrs='0.29 / W' sa=0 sb=0 sd=0 mult=1 m=1
XM4 VN Vbn Vbp GND sky130_fd_pr__nfet_01v8 L={isourcelen} W={isourcewid} nf=1 ad='int((nf+1)/2) * W/nf * 0.29'
+ as='int((nf+2)/2) * W/nf * 0.29' pd='2*int((nf+1)/2) * (W/nf + 0.29)' ps='2*int((nf+2)/2) * (W/nf + 0.29)'
+ nrd='0.29 / W' nrs='0.29 / W' sa=0 sb=0 sd=0 mult=1 m=1
XM6 Vbn Vbn VN GND sky130_fd_pr__nfet_01v8 L={isourcelen} W={isourcewid} nf=1 ad='int((nf+1)/2) * W/nf * 0.29'
+ as='int((nf+2)/2) * W/nf * 0.29' pd='2*int((nf+1)/2) * (W/nf + 0.29)' ps='2*int((nf+2)/2) * (W/nf + 0.29)'
+ nrd='0.29 / W' nrs='0.29 / W' sa=0 sb=0 sd=0 mult=1 m=1
.ends

.GLOBAL VDD
.GLOBAL GND
.end
